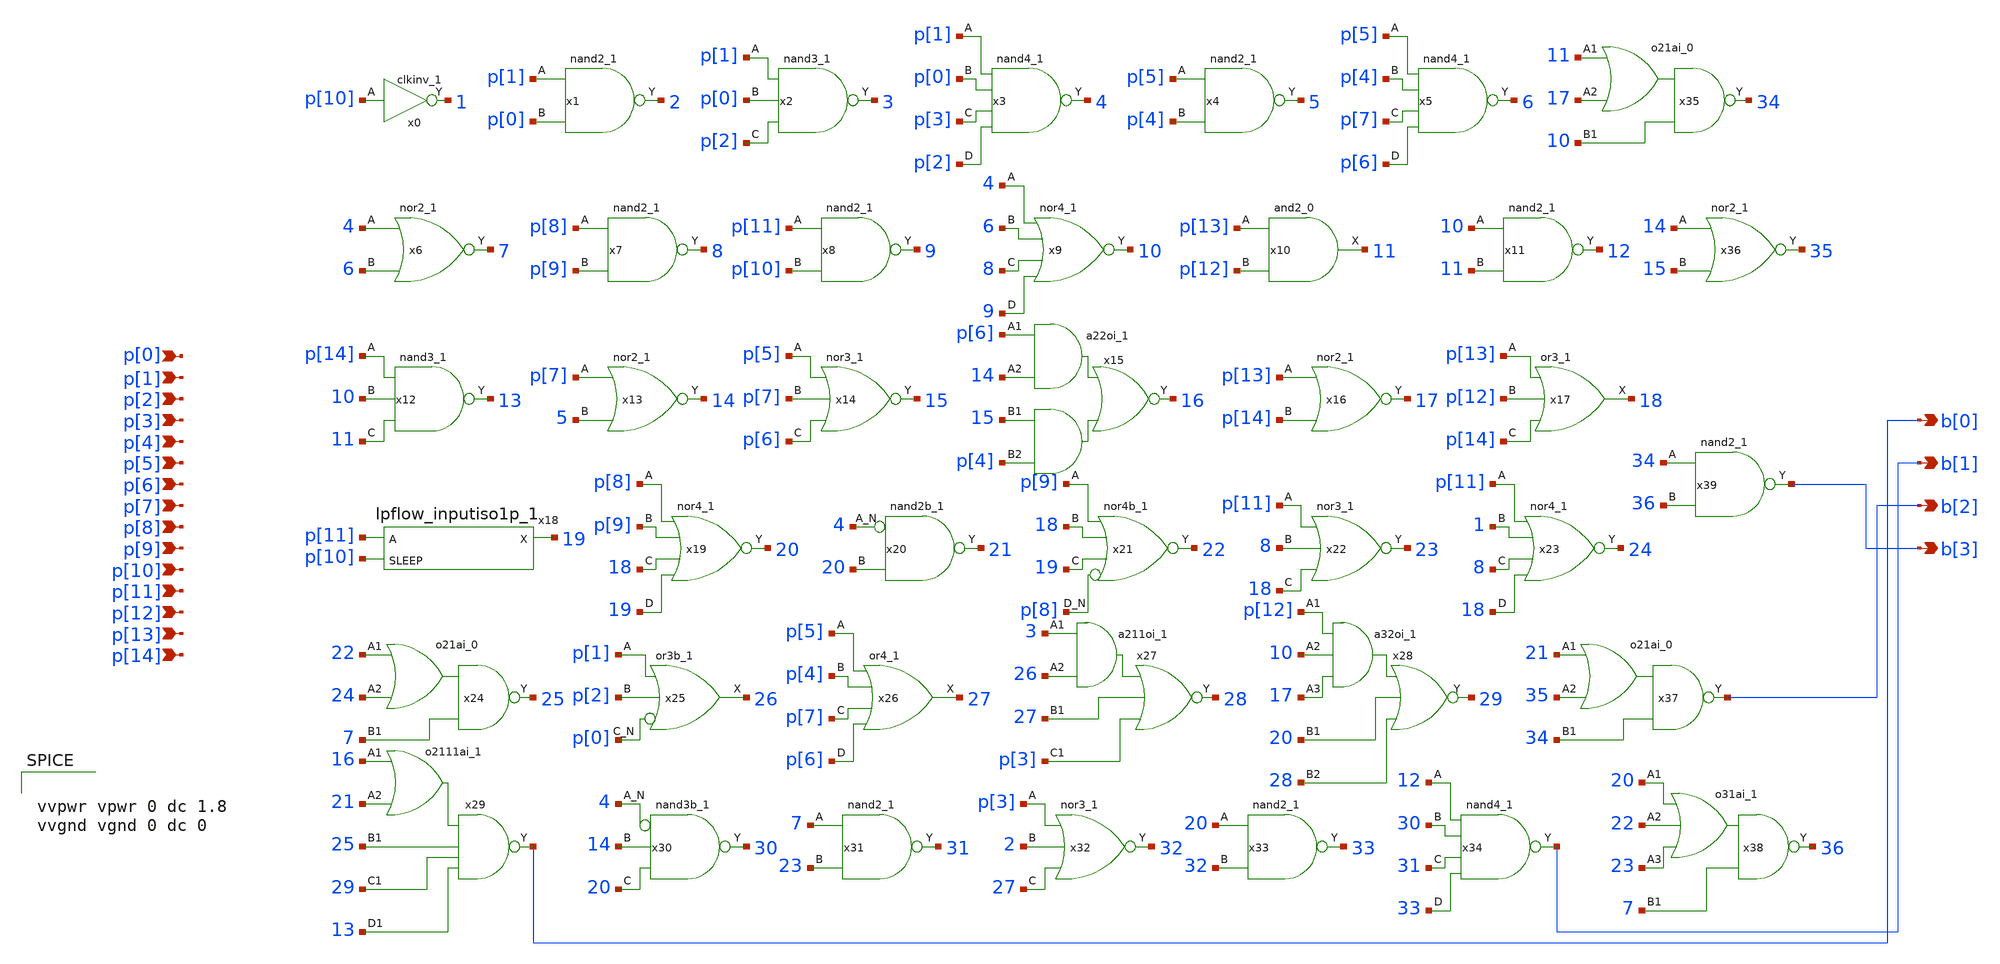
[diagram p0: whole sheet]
** sch_path: xschem/Vth_sch/Symbol/therm.sch
**.subckt therm b[0] p[0] p[1] p[2] p[3] p[4] p[5] p[6] p[7] p[8] p[9] p[10] p[11] p[12] p[13] p[14]
*+ b[1] b[2] b[3]
*.opin b[0]
*.ipin p[0]
*.ipin p[1]
*.ipin p[2]
*.ipin p[3]
*.ipin p[4]
*.ipin p[5]
*.ipin p[6]
*.ipin p[7]
*.ipin p[8]
*.ipin p[9]
*.ipin p[10]
*.ipin p[11]
*.ipin p[12]
*.ipin p[13]
*.ipin p[14]
*.opin b[1]
*.opin b[2]
*.opin b[3]
x0 p[10] VGND VNB VPB VPWR 1 sky130_fd_sc_hd__clkinv_1
x1 p[1] p[0] VGND VNB VPB VPWR 2 sky130_fd_sc_hd__nand2_1
x2 p[1] p[0] p[2] VGND VNB VPB VPWR 3 sky130_fd_sc_hd__nand3_1
x3 p[1] p[0] p[3] p[2] VGND VNB VPB VPWR 4 sky130_fd_sc_hd__nand4_1
x4 p[5] p[4] VGND VNB VPB VPWR 5 sky130_fd_sc_hd__nand2_1
x5 p[5] p[4] p[7] p[6] VGND VNB VPB VPWR 6 sky130_fd_sc_hd__nand4_1
x6 4 6 VGND VNB VPB VPWR 7 sky130_fd_sc_hd__nor2_1
x7 p[8] p[9] VGND VNB VPB VPWR 8 sky130_fd_sc_hd__nand2_1
x8 p[11] p[10] VGND VNB VPB VPWR 9 sky130_fd_sc_hd__nand2_1
x9 4 6 8 9 VGND VNB VPB VPWR 10 sky130_fd_sc_hd__nor4_1
x10 p[13] p[12] VGND VNB VPB VPWR 11 sky130_fd_sc_hd__and2_0
x11 10 11 VGND VNB VPB VPWR 12 sky130_fd_sc_hd__nand2_1
x12 p[14] 10 11 VGND VNB VPB VPWR 13 sky130_fd_sc_hd__nand3_1
x13 p[7] 5 VGND VNB VPB VPWR 14 sky130_fd_sc_hd__nor2_1
x14 p[5] p[7] p[6] VGND VNB VPB VPWR 15 sky130_fd_sc_hd__nor3_1
x15 p[6] 14 15 p[4] VGND VNB VPB VPWR 16 sky130_fd_sc_hd__a22oi_1
x16 p[13] p[14] VGND VNB VPB VPWR 17 sky130_fd_sc_hd__nor2_1
x17 p[13] p[12] p[14] VGND VNB VPB VPWR 18 sky130_fd_sc_hd__or3_1
x18 p[11] p[10] VGND VNB VPB VPWR 19 sky130_fd_sc_hd__lpflow_inputiso1p_1
x19 p[8] p[9] 18 19 VGND VNB VPB VPWR 20 sky130_fd_sc_hd__nor4_1
x20 4 20 VGND VNB VPB VPWR 21 sky130_fd_sc_hd__nand2b_1
x21 p[9] 18 19 p[8] VGND VNB VPB VPWR 22 sky130_fd_sc_hd__nor4b_1
x22 p[11] 8 18 VGND VNB VPB VPWR 23 sky130_fd_sc_hd__nor3_1
x23 p[11] 1 8 18 VGND VNB VPB VPWR 24 sky130_fd_sc_hd__nor4_1
x24 22 24 7 VGND VNB VPB VPWR 25 sky130_fd_sc_hd__o21ai_0
x25 p[1] p[2] p[0] VGND VNB VPB VPWR 26 sky130_fd_sc_hd__or3b_1
x26 p[5] p[4] p[7] p[6] VGND VNB VPB VPWR 27 sky130_fd_sc_hd__or4_1
x27 3 26 27 p[3] VGND VNB VPB VPWR 28 sky130_fd_sc_hd__a211oi_1
x28 p[12] 10 17 20 28 VGND VNB VPB VPWR 29 sky130_fd_sc_hd__a32oi_1
x29 16 21 25 29 13 VGND VNB VPB VPWR b[0] sky130_fd_sc_hd__o2111ai_1
x30 4 14 20 VGND VNB VPB VPWR 30 sky130_fd_sc_hd__nand3b_1
x31 7 23 VGND VNB VPB VPWR 31 sky130_fd_sc_hd__nand2_1
x32 p[3] 2 27 VGND VNB VPB VPWR 32 sky130_fd_sc_hd__nor3_1
x33 20 32 VGND VNB VPB VPWR 33 sky130_fd_sc_hd__nand2_1
x34 12 30 31 33 VGND VNB VPB VPWR b[1] sky130_fd_sc_hd__nand4_1
x35 11 17 10 VGND VNB VPB VPWR 34 sky130_fd_sc_hd__o21ai_0
x36 14 15 VGND VNB VPB VPWR 35 sky130_fd_sc_hd__nor2_1
x37 21 35 34 VGND VNB VPB VPWR b[2] sky130_fd_sc_hd__o21ai_0
x38 20 22 23 7 VGND VNB VPB VPWR 36 sky130_fd_sc_hd__o31ai_1
x39 34 36 VGND VNB VPB VPWR b[3] sky130_fd_sc_hd__nand2_1
**** begin user architecture code


vvpwr vpwr 0 dc 1.8
vvgnd vgnd 0 dc 0


**** end user architecture code
**.ends
.end
